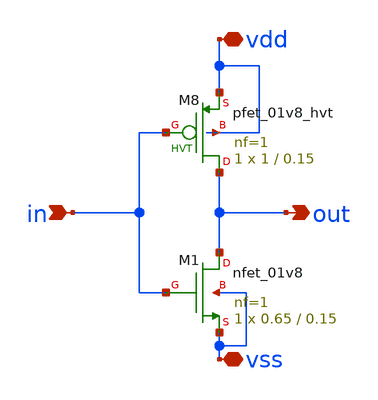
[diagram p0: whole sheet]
** sch_path: sample/xschem/inv.sch
**.subckt inv vdd in out vss
*.iopin vdd
*.ipin in
*.opin out
*.iopin vss
XM1 out in vss vss sky130_fd_pr__nfet_01v8 L=0.15 W=0.65 nf=1 ad='int((nf+1)/2) * W/nf * 0.29' as='int((nf+2)/2) * W/nf * 0.29'
+ pd='2*int((nf+1)/2) * (W/nf + 0.29)' ps='2*int((nf+2)/2) * (W/nf + 0.29)' nrd='0.29 / W' nrs='0.29 / W'
+ sa=0 sb=0 sd=0 mult=1 m=1
XM8 out in vdd vdd sky130_fd_pr__pfet_01v8_hvt L=0.15 W=1 nf=1 ad='int((1 + 1)/2) * 1 / 1 * 0.29' as='int((1 + 2)/2) * 1 / 1 * 0.29'
+ pd='2*int((1 + 1)/2) * (1 / 1 + 0.29)' ps='2*int((1 + 2)/2) * (1 / 1 + 0.29)' nrd='0.29 / 1 ' nrs='0.29 / 1 '
+ sa=0 sb=0 sd=0 mult=1 m=1
**.ends
.end
